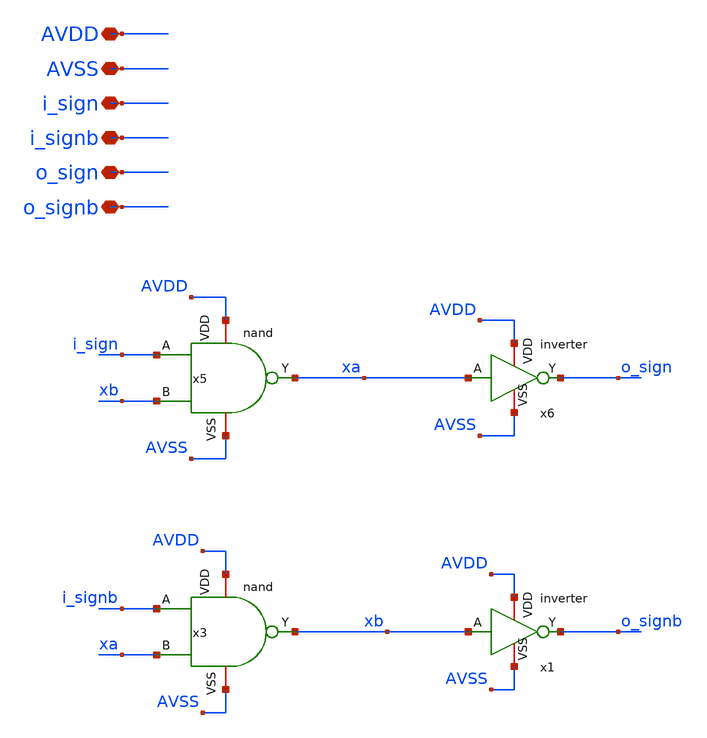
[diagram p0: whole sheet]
** sch_path: current_generator/analog/DAC/schematics/non_overlap_gold.sch
**.subckt non_overlap_gold AVDD AVSS i_sign i_signb o_sign o_signb
*.iopin AVDD
*.iopin AVSS
*.iopin i_sign
*.iopin i_signb
*.iopin o_sign
*.iopin o_signb
x5 AVDD AVSS i_sign xb xa nand
x6 xa o_sign AVDD AVSS inverter
x3 AVDD AVSS i_signb xa xb nand
x1 xb o_signb AVDD AVSS inverter
**.ends

* expanding   symbol:  nand.sym # of pins=5
** sym_path: current_generator/analog/DAC/schematics/nand.sym
** sch_path: current_generator/analog/DAC/schematics/nand.sch
.subckt nand VDD VSS A B Y
*.opin Y
*.ipin A
*.iopin VDD
*.iopin VSS
*.ipin B
XMN0 net1 B VSS VSS sg13_lv_nmos w=1.44u l=130.00n ng=2 m=1 mm_ok=1
XMP0 Y B VDD VDD sg13_lv_pmos w=2.24u l=130.00n ng=2 m=1 mm_ok=1
XMN1 Y A net1 VSS sg13_lv_nmos w=1.44u l=130.00n ng=2 m=1 mm_ok=1
XMP1 Y A VDD VDD sg13_lv_pmos w=2.24u l=130.00n ng=2 m=1 mm_ok=1
.ends


* expanding   symbol:  inverter.sym # of pins=4
** sym_path: current_generator/analog/DAC/schematics/inverter.sym
** sch_path: current_generator/analog/DAC/schematics/inverter.sch
.subckt inverter A Y VDD VSS
*.opin Y
*.ipin A
*.iopin VDD
*.iopin VSS
MMN0 Y A VSS VSS sg13_lv_nmos w=740.00n l=130.00n ng=1 m=1 mm_ok=1
MMP0 Y A VDD VDD sg13_lv_pmos w=1.12u l=130.00n ng=1 m=1 mm_ok=1
.ends

.end
